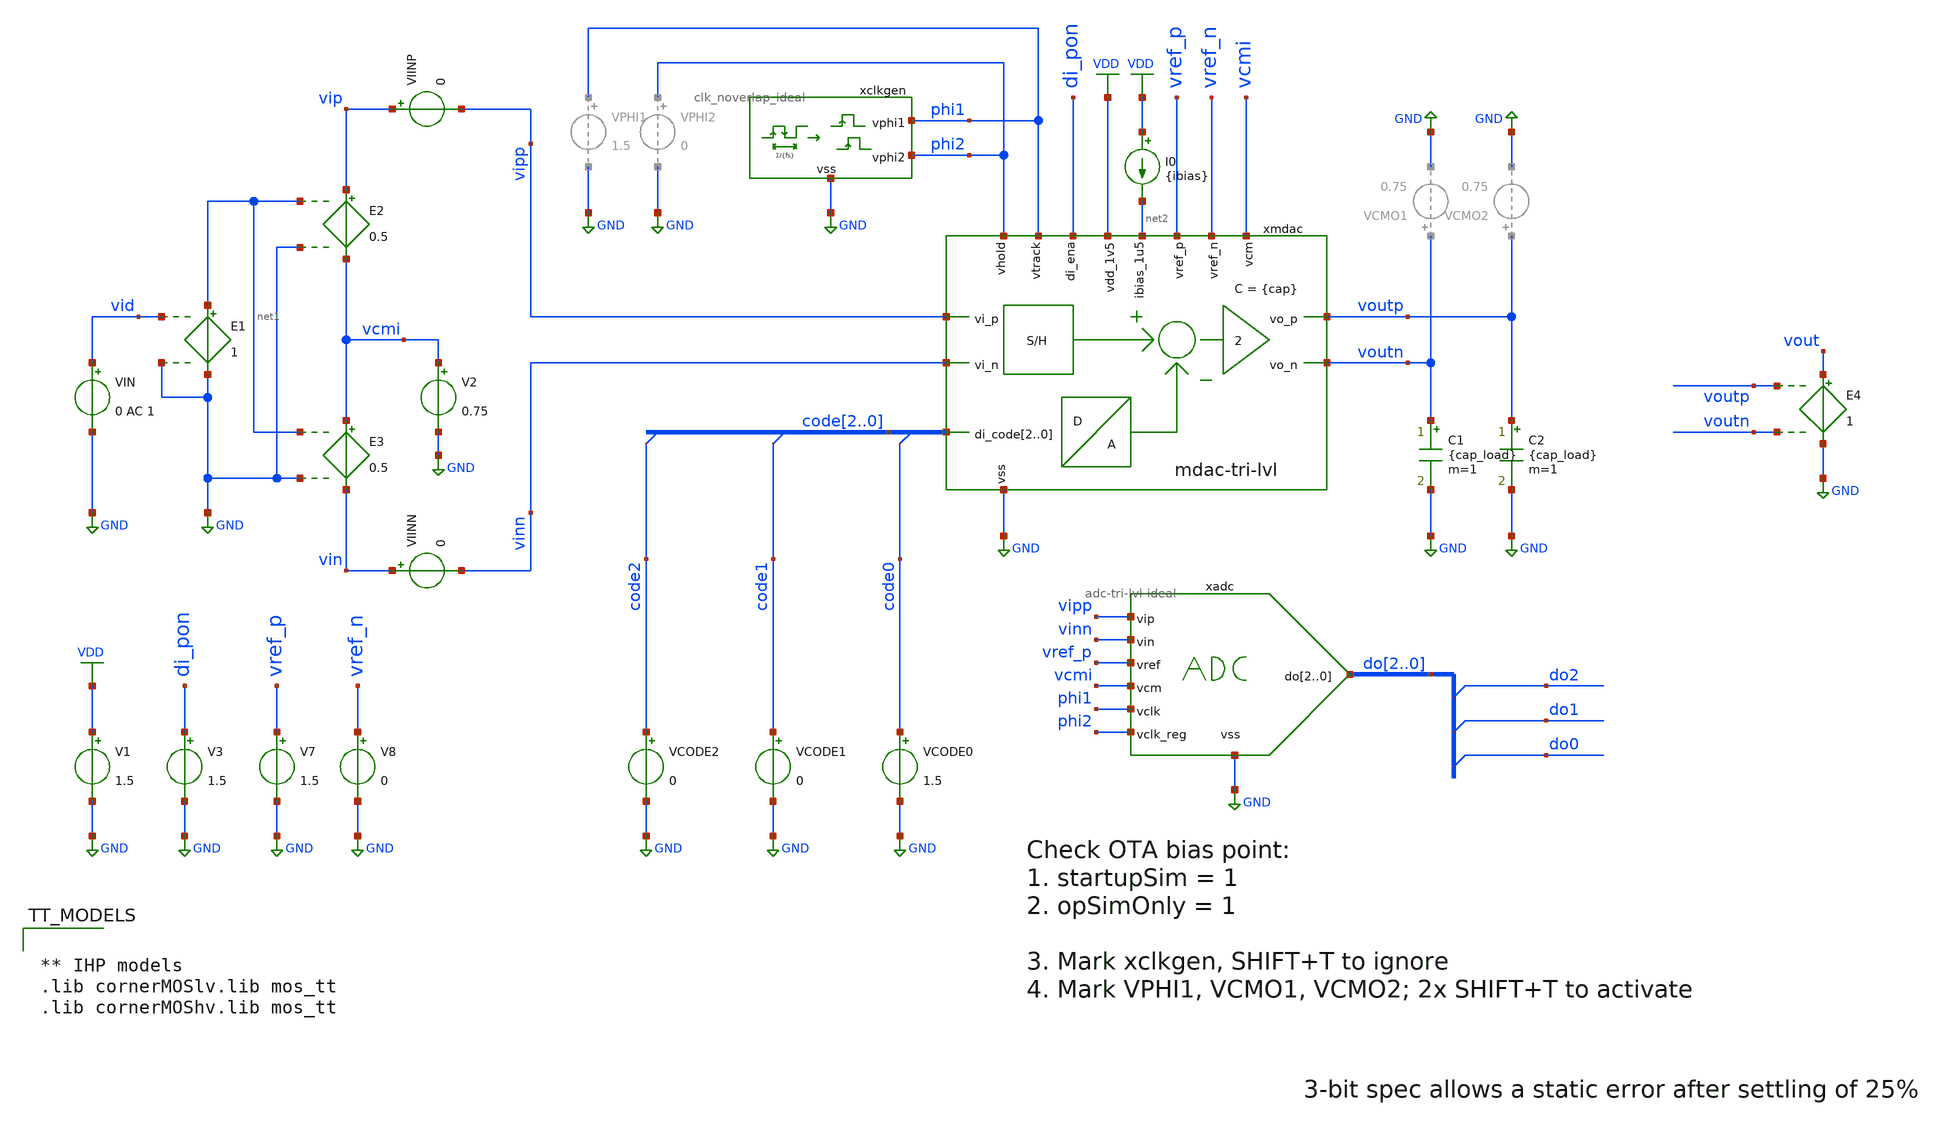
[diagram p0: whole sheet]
** sch_path: xschem/mdac-tri-lvl_tb-tran.sch
* xschem/ota-5t-fd.sch:
* (c) 2025 M. Koefinger
**.subckt mdac-tri-lvl_tb-tran
V1 VDD GND 1.5
V3 di_pon GND 1.5
V2 vcmi GND 0.75
E3 vcmi vin net1 GND 0.5
E2 vip vcmi net1 GND 0.5
VIN vid GND 0 AC 1
E1 net1 GND vid GND 1
VIINP vip vipp 0
VIINN vin vinn 0
E4 vout GND voutp voutn 1
xclkgen phi1 phi2 GND clk_noverlap_ideal fs={fs} tnover=50n tdelay=0 trf=5n
VCODE2 code2 GND 0
VCODE1 code1 GND 0
VCODE0 code0 GND 1.5
C1 voutn GND {cap_load} m=1
C2 voutp GND {cap_load} m=1
V7 vref_p GND 1.5
V8 vref_n GND 0
I0 VDD net2 {ibias}
xmdac VDD net2 phi2 phi1 vipp code2 code1 code0 vref_p vref_n voutp vcmi voutn vinn di_pon GND
+ mdac-tri-lvl
xadc do2 do1 do0 vipp vinn vref_p vcmi phi1 GND phi2 adc-tri-lvl-ideal
**** begin user architecture code


.include mdac-tri-lvl_tb-tran.save
.options savecurrents
.options method=gear reltol=.005
.options sparse
.param fs=2Meg
.param ibias=3u
.param cap=100f
.param cap_load = 100f
.param ron=1
.param roff=1G
.ic v(xmdac.vgndp) = 1 v(xmdac.vgndn) = 1 v(voutp) = 0.75 v(voutn) = 0.75 v(phi1)=1.5

.control
save voutp voutn vinn vipp vid vcmi phi1 phi2 code[2:0] vout vref_p vref_n di_pon vdd
** mdac saves
save xmdac.vdac_p xmdac.vdac_n xmdac.vgndp xmdac.vgndn xmdac.vfb xmdac.vbp
save xmdac.xc1.vc_p xmdac.xc2.vc_p xmdac.xc3.vc_p xmdac.xc4.vc_p
** mdac ota saves
save xmdac.xota.tail xmdac.xota.ena xmdac.xota.ena_n xmdac.xota.gate_n
save do2 do1 do0

set wr_singlescale
set wr_vecnames
option numdgt=3

** Sim options
set startupSim = 0
set opSimOnly = 0

** System Specs
let err_max = 0.25
let fs = 2Meg

** Startup
let n_per_startup = 100
let tsettle = 1/fs/2
let t_rf = 0.01/fs
let t_delay = n_per_startup/fs
let t_per = tsettle

** Default Input Config
alter @VIN[DC] = 0.0
alter @VCODE2[DC] = 0.0
alter @VCODE1[DC] = 0.0
alter @VCODE0[DC] = 1.5

** Transient Sim Options
let tstep = 0.1*t_rf
if $startupSim eq 1
	let tstart = 0
	let tstop = t_delay
else
	let tstart = t_delay
	let tstop = 20*t_per+t_delay
	let vi = 1
	let vref = 1.5
	alter @VIN[DC] = vi
	alter @VCODE0[DC] = 0
	alter @VCODE1[DC] = 0
	alter @VCODE2[DC] = 1.5
	*let vi = -1
	*let vref = -1.5
	*alter @VCODE1[DC] = 1.5
	*alter @VCODE2[DC] = 0
end

** Main Simulations
if $opSimOnly eq 0
	*optran 0 0 0 $&t_per $&t_delay 0
	tran $&tstep $&tstop $&tstart

	setplot tran1
	let vid = v(vipp,vinn)
	let vip_mdac = v(vipp,xmdac.vgndn)
	let vin_mdac = v(vinn,xmdac.vgndp)
	let vcmo = (voutp+voutn)/2
	let vcmi = (xmdac.vgndp+xmdac.vgndn)/2
	let vod = v(vout)
	let vdacd = xmdac.vdac_n-xmdac.vdac_p
	let vc1 = v(xmdac.xc1.vc_p,xmdac.vgndn)
	let vc2 = v(xmdac.xc2.vc_p,xmdac.vgndn)
	let vc3 = v(xmdac.xc3.vc_p,xmdac.vgndp)
	let vc4 = v(xmdac.xc4.vc_p,xmdac.vgndp)
	let vop_mdac = v(voutp,vcmi)
	let von_mdac = v(voutn,vcmi)
	let settle_goal = 2*vid-vdacd
	let err = (settle_goal-vod)/settle_goal

	write mdac-tri-lvl_tb-tran.raw
	set appendwrite

	plot vid vod phi2 settle_goal
	plot err*100 phi2*100
end
if $opSimOnly eq 1 and $startupSim eq 1
	save all
end
alter @VIN[DC] = 0
alter @VCODE2[DC] = 0.0
alter @VCODE1[DC] = 0.0
alter @VCODE0[DC] = 1.5
optran 0 0 0 0.1u 1m 0
op
remzerovec
write mdac-tri-lvl_tb-tran.raw
.endc



** IHP models
.lib cornerMOSlv.lib mos_tt
.lib cornerMOShv.lib mos_tt


**** end user architecture code
**.ends

* expanding   symbol:  clk_noverlap_ideal.sym # of pins=3
** sym_path: xschem/clk_noverlap_ideal.sym
** sch_path: xschem/clk_noverlap_ideal.sch
.subckt clk_noverlap_ideal vphi1 vphi2 vss  fs=100Meg tnover=2n tdelay=0 trf=0.1n
*.iopin vss
*.opin vphi1
*.opin vphi2
V1 vphi1 vss 0 PULSE 0 1.5 {tdelay} {trf} {trf} {0.5/{fs}-{tnover}} {1/{fs}} 0
V2 vphi2 vss 0 PULSE 0 1.5 {{tdelay}+{0.5/{fs}}} {trf} {trf} {0.5/{fs}-{tnover}} {1/{fs}} 0
.ends


* expanding   symbol:  mdac-tri-lvl.sym # of pins=14
** sym_path: xschem/mdac-tri-lvl.sym
** sch_path: xschem/mdac-tri-lvl.sch
.subckt mdac-tri-lvl vdd_1v5 ibias_1u5 vhold vtrack vi_p di_code2 di_code1 di_code0 vref_p vref_n
+ vo_p vcm vo_n vi_n di_ena vss
*.ipin vi_p
*.ipin vi_n
*.ipin di_ena
*.iopin vss
*.iopin vdd_1v5
*.ipin ibias_1u5
*.opin vo_n
*.opin vo_p
*.ipin vref_p
*.ipin vref_n
*.ipin vcm
*.ipin di_code2,di_code1,di_code0
*.ipin vtrack
*.ipin vhold
xota vdd_1v5 vfb vo_p vo_n vgndp vgndn ibias_1u5 di_ena vss vbp ota-5t-fd
S1 vgndn vo_p vtrack vss SW1
xcmfb vhold vtrack vss vo_p vcm vbp vfb vo_n cmfb_sc cap={cap} div=10
S2 vgndp vo_n vtrack vss SW1
xc1 vhold vo_p vgndn vi_p vtrack vss sw_cap cap={cap} ron=1 roff=1G
xc2 vhold vdac_n vgndn vi_p vtrack vss sw_cap cap={cap} ron=1 roff=1G
xc3 vhold vo_n vgndp vi_n vtrack vss sw_cap cap={cap} ron=1 roff=1G
xc4 vhold vdac_p vgndp vi_n vtrack vss sw_cap cap={cap} ron=1 roff=1G
xsw1 di_code2 di_code1 di_code0 vref_p vref_n vdac_n vcm vss sw_dac ron=1 roff=1G
xsw2 di_code2 di_code1 di_code0 vref_n vref_p vdac_p vcm vss sw_dac ron=1 roff=1G
.ends


* expanding   symbol:  adc-tri-lvl-ideal.sym # of pins=8
** sym_path: xschem/adc-tri-lvl-ideal.sym
** sch_path: xschem/adc-tri-lvl-ideal.sch
.subckt adc-tri-lvl-ideal do2 do1 do0 vip vin vref vcm vclk vss vclk_reg
*.iopin vss
*.ipin vip
*.ipin vin
*.ipin vref
*.ipin vcm
*.ipin vclk
*.opin do2,do1,do0
*.ipin vclk_reg
xcomp1 D1 vip vin vcm vref vss comp-macro
xcomp2 D0 vip vin vref vcm vss comp-macro
**** begin user architecture code


a31 Q_REG0 CLK_REG NULL NULL %d(Q0 NQ0) dff1
a32 Q_REG1 CLK_REG NULL NULL %d(Q1 NQ1) dff1


**** end user architecture code
**** begin user architecture code


.model adc_buf adc_bridge(in_low=0.7499 in_high=0.7501)
.model dac1 dac_bridge(out_low = 0 out_high = 1.5 out_undef = 0 input_load = 0.1e-15 t_rise =
+ 0.01e-9 t_fall = 0.01e-9)
.model inv1 d_inverter(rise_delay = 0.01e-9 fall_delay = 0.01e-9 input_load = 0.1e-15)
.model and1 d_and(rise_delay = 0.01e-9 fall_delay = 0.01e-9 input_load = 0.01e-15)
.model dff1 d_dff(clk_delay = 0.01e-9 set_delay = 0.01e-9 reset_delay = 0.01e-9 ic = 0 rise_delay =
+ 0.01e-9 fall_delay = 0.01e-9)
.model dlatch1 d_dlatch(data_delay = 0.01e-9 enable_delay = 0.01e-9 set_delay = 0.01e-9 reset_delay
+ = 0.01e-9 ic = 0 rise_delay = 0.01e-9 fall_delay = 0.01e-9)

**** end user architecture code
A1 [ vclk ] [ CLK ] adc_buf
A3 [ H1 ] [ do1 ] dac1
A4 [ H2 ] [ do2 ] dac1
**** begin user architecture code


a23 [NQ1 Q0] %d(H0) and1
a24 [NQ1 NQ0] %d(H1) and1
a25 [Q1 Q0] %d(H2) and1


**** end user architecture code
A2 [ H0 ] [ do0 ] dac1
**** begin user architecture code


a21 D0 CLK NULL NULL %d(Q_REG0 NQ_REG0) dlatch1
a22 D1 CLK NULL NULL %d(Q_REG1 NQ_REG1) dlatch1


**** end user architecture code
A5 [ vclk_reg ] [ CLK_REG ] adc_buf
.ends


* expanding   symbol:  ota-5t-fd.sym # of pins=10
** sym_path: xschem/ota-5t-fd.sym
** sch_path: xschem/ota-5t-fd.sch
.subckt ota-5t-fd vdd vfb voutp voutn vinp vinn ibias_1u5 d_ena vss vbp
*.ipin ibias_1u5
*.iopin vdd
*.iopin vss
*.ipin vinp
*.ipin vinn
*.opin voutn
*.ipin d_ena
*.opin voutp
*.ipin vfb
*.opin vbp
XMN3 tail gate_n vss vss sg13_lv_nmos w=2.5u l=0.5u ng=5 m=1 mm_ok=1
XMP2 voutp vfb vdd vdd sg13_lv_pmos w=0.5u l=0.5u ng=1 m=1 mm_ok=1
XMN1 voutn vinp tail vss sg13_lv_nmos w=5.5u l=0.5u ng=11 m=1 mm_ok=1
XMN2 voutp vinn tail vss sg13_lv_nmos w=5.5u l=0.5u ng=11 m=1 mm_ok=1
XMP1 voutn vfb vdd vdd sg13_lv_pmos w=0.5u l=0.5u ng=1 m=1 mm_ok=1
XMN4 ibias_1u5 gate_n vss vss sg13_lv_nmos w=1.5u l=0.5u ng=3 m=1 mm_ok=1
XMN5 gate_n ena_n vss vss sg13_lv_nmos w=0.5u l=0.13u ng=1 m=1 mm_ok=1
XMPSW1 vfb ena vdd vdd sg13_lv_pmos w=1.5u l=0.13u ng=1 m=1 mm_ok=1
XMN8 ena ena_n vss vss sg13_lv_nmos w=0.5u l=0.13u ng=1 m=1 mm_ok=1
XMP5 ena ena_n vdd vdd sg13_lv_pmos w=1.5u l=0.13u ng=1 m=1 mm_ok=1
XMN6 ibias_1u5 ena gate_n vss sg13_lv_nmos w=0.5u l=0.13u ng=1 m=1 mm_ok=1
XMN7 ena_n d_ena vss vss sg13_lv_nmos w=0.5u l=0.13u ng=1 m=1 mm_ok=1
XMP4 ena_n d_ena vdd vdd sg13_lv_pmos w=1.5u l=0.13u ng=1 m=1 mm_ok=1
XMN9 vbp gate_n vss vss sg13_lv_nmos w=1u l=0.5u ng=2 m=1 mm_ok=1
XMP3 vbp vbp vdd vdd sg13_lv_pmos w=0.5u l=0.5u ng=1 m=1 mm_ok=1
.ends


* expanding   symbol:  cmfb_sc.sym # of pins=8
** sym_path: xschem/cmfb_sc.sym
** sch_path: xschem/cmfb_sc.sch
.subckt cmfb_sc vphi2 vphi1 vss vo_p vcm vbias vfb vo_n  cap=100f div=10
*.ipin vcm
*.ipin vphi2
*.ipin vphi1
*.iopin vss
*.ipin vbias
*.iopin vo_p
*.iopin vo_n
*.opin vfb
C1 vo_p vfb 100f m=1
C2 net1 net2 10f m=1
C3 vfb vo_n 100f m=1
C4 net2 net3 10f m=1
S3 net1 vo_p vphi1 vss SW1
S4 vcm net1 vphi2 vss SW1
S6 net2 vfb vphi1 vss SW1
S7 vbias net2 vphi2 vss SW1
S9 net3 vo_n vphi1 vss SW1
S10 vcm net3 vphi2 vss SW1
.ends


* expanding   symbol:  sw_cap.sym # of pins=6
** sym_path: xschem/sw_cap.sym
** sch_path: xschem/sw_cap.sch
.subckt sw_cap di_1 vi1 vo vi2 di_2 vss  cap=100f ron=1 roff=1G
*.ipin di_1
*.ipin di_2
*.iopin vi1
*.iopin vi2
*.iopin vo
*.iopin vss
C1 vc_p vo {cap} m=1
S1 vi1 vc_p di_1 vss SW1
S2 vi2 vc_p di_2 vss SW1
.ends


* expanding   symbol:  sw_dac.sym # of pins=6
** sym_path: xschem/sw_dac.sym
** sch_path: xschem/sw_dac.sch
.subckt sw_dac di_code2 di_code1 di_code0 vref_p vref_n vo vcm vss  ron=1 roff=1G
*.ipin di_code2,di_code1,di_code0
*.iopin vref_p
*.iopin vref_n
*.iopin vo
*.iopin vss
*.iopin vcm
S1 vref_p vo di_code2 vss SW1
S2 vref_n vo di_code1 vss SW1
S3 vcm vo di_code0 vss SW1
.ends


* expanding   symbol:  comp-macro.sym # of pins=6
** sym_path: xschem/comp-macro.sym
** sch_path: xschem/comp-macro.sch
.subckt comp-macro do vip_1 vin_1 vip_2 vin_2 vss
*.iopin vss
*.ipin vip_1
*.ipin vin_1
*.ipin vip_2
*.ipin vin_2
*.opin do
A1 [ net1 ] [ do ] comp0
E1 net1 net2 vip_1 vin_1 1
E2 net2 vss vip_2 vin_2 1
**** begin user architecture code

.model comp0 adc_bridge(in_low=-0.0001 in_high=0.0001)

**** end user architecture code
.ends

.GLOBAL GND
.GLOBAL VDD
**** begin user architecture code
.MODEL SW1 SW( VT=0.75 VH=0.01 RON=ron ROFF=roff )
**** end user architecture code
.end
